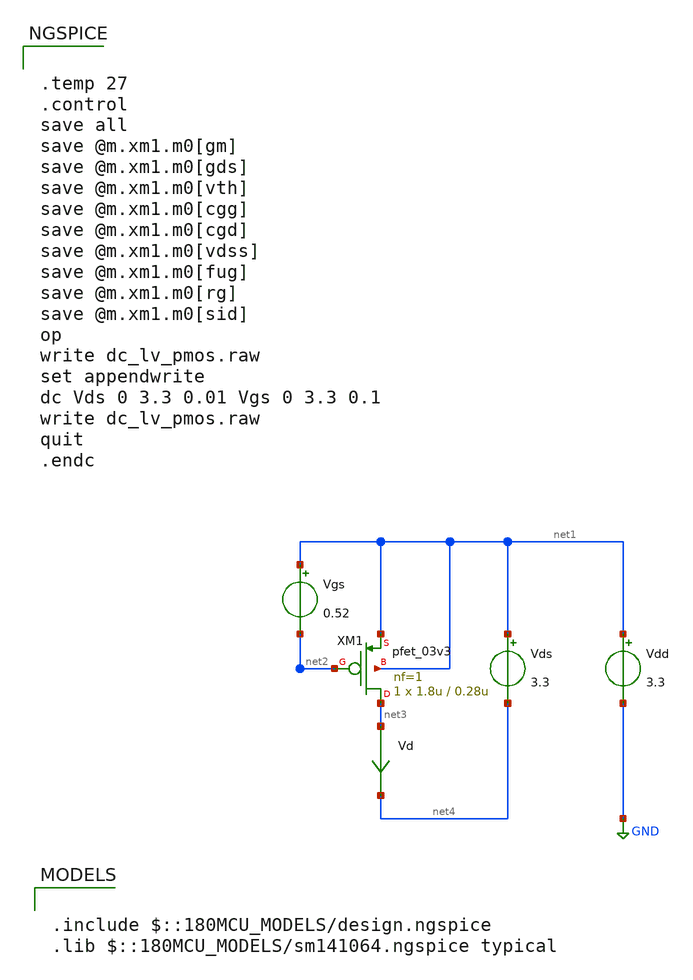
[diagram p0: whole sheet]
** sch_path: Modulo_Analogico/Laboratorios/Lab1/dc_lv_pmos.sch
**.subckt dc_lv_pmos
Vgs net1 net2 0.52
Vds net1 net4 3.3
Vd net3 net4 0
.save i(vd)
Vdd net1 GND 3.3
XM1 net3 net2 net1 net1 pfet_03v3 L=0.28u W=1.8u nf=1 ad='int((nf+1)/2) * W/nf * 0.18u' as='int((nf+2)/2) * W/nf * 0.18u'
+ pd='2*int((nf+1)/2) * (W/nf + 0.18u)' ps='2*int((nf+2)/2) * (W/nf + 0.18u)' nrd='0.18u / W' nrs='0.18u / W'
+ sa=0 sb=0 sd=0 m=1
**** begin user architecture code


.temp 27
.control
save all
save @m.xm1.m0[gm]
save @m.xm1.m0[gds]
save @m.xm1.m0[vth]
save @m.xm1.m0[cgg]
save @m.xm1.m0[cgd]
save @m.xm1.m0[vdss]
save @m.xm1.m0[fug]
save @m.xm1.m0[rg]
save @m.xm1.m0[sid]
op
write dc_lv_pmos.raw
set appendwrite
dc Vds 0 3.3 0.01 Vgs 0 3.3 0.1
write dc_lv_pmos.raw
quit
.endc



.include $::180MCU_MODELS/design.ngspice
.lib $::180MCU_MODELS/sm141064.ngspice typical

**** end user architecture code
**.ends
.GLOBAL GND
.end
